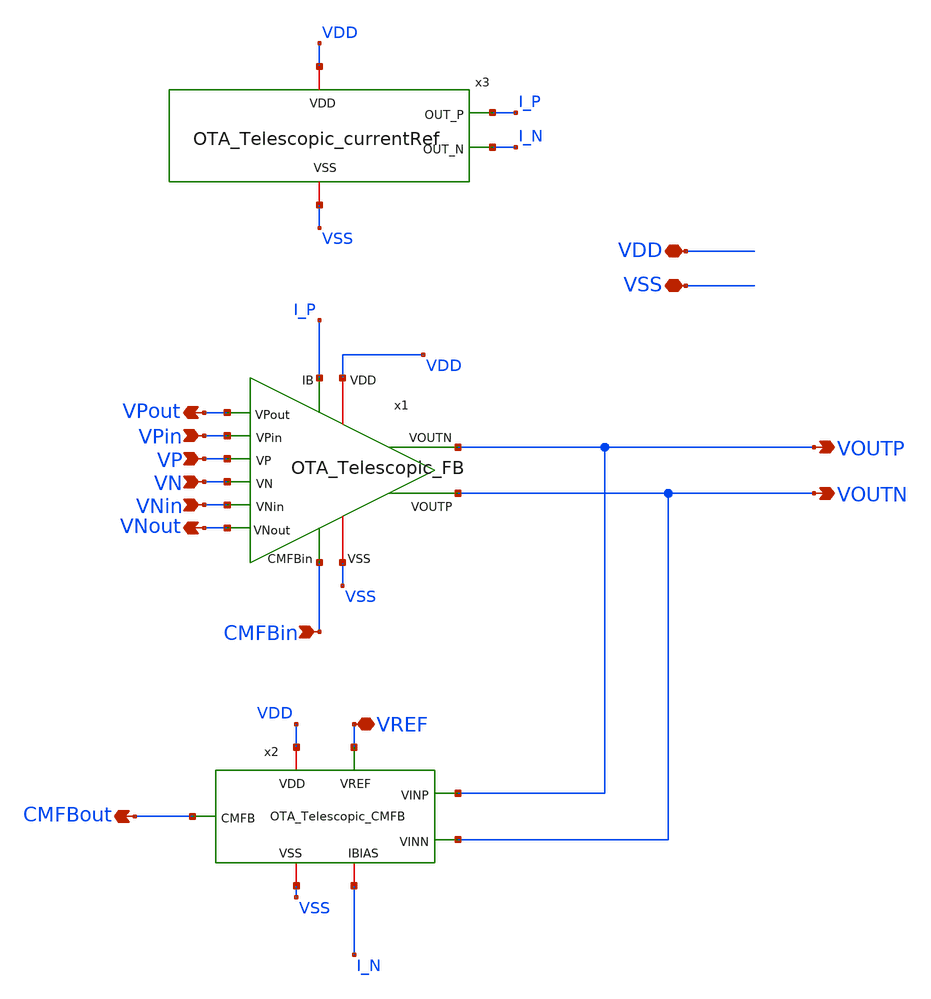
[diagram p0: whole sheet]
** sch_path: OTA_Telescopic_TEST/OTA_Telescopic_TOP_wp.sch
**.subckt OTA_Telescopic_TOP_wp VP VN VOUTP VOUTN VPin VNin VPout VNout VDD VSS VREF CMFBin CMFBout
*.ipin VP
*.ipin VN
*.opin VOUTP
*.opin VOUTN
*.ipin VPin
*.ipin VNin
*.opin VPout
*.opin VNout
*.iopin VDD
*.iopin VSS
*.iopin VREF
*.ipin CMFBin
*.opin CMFBout
x3 VDD I_P I_N VSS OTA_Telescopic_currentRef
x2 VDD VREF VOUTN VOUTP I_N CMFBout VSS OTA_Telescopic_CMFB
x1 I_P VPout VP VPin VOUTN VDD VOUTP VSS VNin VNout VN CMFBin OTA_Telescopic_FB
**.ends

* expanding   symbol:  OTA_Telescopic_currentRef.sym # of pins=4
** sym_path: OTA_Telescopic/OTA_Telescopic_currentRef.sym
** sch_path: OTA_Telescopic/OTA_Telescopic_currentRef.sch
.subckt OTA_Telescopic_currentRef VDD OUT_P OUT_N VSS
*.iopin VDD
*.iopin VSS
*.opin OUT_P
*.opin OUT_N
XM3 OUT_P OUT_P VDD VDD sg13_lv_pmos w=12u l=2.5u ng=2 m=1 mm_ok=1
XM2 OUT_P OUT_N net1 VSS sg13_lv_nmos w=12u l=6.4u ng=2 m=8 mm_ok=1
XM4 OUT_N OUT_P VDD VDD sg13_lv_pmos w=12u l=2.5u ng=2 m=1 mm_ok=1
XM1 OUT_N OUT_N VSS VSS sg13_lv_nmos w=12u l=6.4u ng=2 m=1 mm_ok=1
XM5 OUT_P OUT_P OUT_N VSS sg13_lv_nmos w=2u l=1u ng=1 m=1 mm_ok=1
XR2 net1 VSS VSS rppd w=1e-6 l=13.5e-6 m=1 b=0 mm_ok=1
.ends


* expanding   symbol:  OTA_Telescopic_CMFB.sym # of pins=7
** sym_path: OTA_Telescopic_CMFB.sym
** sch_path: OTA_Telescopic_CMFB.sch
.subckt OTA_Telescopic_CMFB VDD VREF VINN VINP IBIAS CMFB VSS
*.iopin VDD
*.iopin VSS
*.opin CMFB
*.ipin VREF
*.iopin IBIAS
*.ipin VINP
*.ipin VINN
XM0 IBIAS IBIAS VDD VDD sg13_lv_pmos w=6u l=0.7u ng=6 m=8 mm_ok=1
XM1 V1 IBIAS VDD VDD sg13_lv_pmos w=6u l=0.7u ng=6 m=24 mm_ok=1
XM2 V2 IBIAS VDD VDD sg13_lv_pmos w=6u l=0.7u ng=6 m=24 mm_ok=1
XM3 CMFB VINP V1 VDD sg13_lv_pmos w=8.995u l=0.35u ng=7 m=4 mm_ok=1
XM4 net1 VREF V1 VDD sg13_lv_pmos w=8.995u l=0.35u ng=7 m=4 mm_ok=1
XM5 net1 VREF V2 VDD sg13_lv_pmos w=8.995u l=0.35u ng=7 m=4 mm_ok=1
XM6 CMFB VINN V2 VDD sg13_lv_pmos w=8.995u l=0.35u ng=7 m=4 mm_ok=1
XM7 net1 net1 VSS VSS sg13_lv_nmos w=29.97u l=0.20u ng=9 m=1 mm_ok=1
XM8 CMFB CMFB VSS VSS sg13_lv_nmos w=29.97u l=0.20u ng=9 m=1 mm_ok=1
.ends


* expanding   symbol:  OTA_Telescopic_FB.sym # of pins=12
** sym_path: OTA_Telescopic_FB.sym
** sch_path: OTA_Telescopic_FB.sch
.subckt OTA_Telescopic_FB IB VPout VP VPin VOUTP VDD VOUTN VSS VNin VNout VN CMFBin
*.ipin VP
*.ipin VN
*.opin VOUTP
*.opin VOUTN
*.ipin VPin
*.ipin VNin
*.opin VPout
*.opin VNout
*.iopin VDD
*.iopin VSS
*.ipin CMFBin
*.ipin IB
x1 VDD CMFBin VOUTN VOUTP VPin VNin VSS IB OTA_Telescopic_core
XR3 VNout VN VSS rppd w=0.6e-6 l=6.73e-6 m=1 b=0 mm_ok=1
XR4 VP VPout VSS rppd w=0.6e-6 l=6.73e-6 m=1 b=0 mm_ok=1
XR5 VPout VOUTP VSS rppd w=0.6e-6 l=19e-6 m=1 b=0 mm_ok=1
XR2 VNout VOUTN VSS rppd w=0.6e-6 l=19e-6 m=1 b=0 mm_ok=1
.ends


* expanding   symbol:  OTA_Telescopic_core.sym # of pins=8
** sym_path: OTA_Telescopic_core.sym
** sch_path: OTA_Telescopic_core.sch
.subckt OTA_Telescopic_core VDD CMFB VOUTP VOUTN VINP VINN VSS IB
*.iopin VDD
*.iopin VSS
*.ipin VINP
*.ipin VINN
*.opin VOUTN
*.opin VOUTP
*.ipin CMFB
*.iopin IB
V2 VB2 VSS 1.5
V3 VB3 VSS 0.7
V4 VB4 VSS 0.49409
V1 VB5 VSS 1.15
* noconn VB2
* noconn VB3
* noconn VB4
* noconn VB5
V5 VB VSS 0.90204
* noconn VB
XM15 VB55 VB55 VDD VDD sg13_lv_pmos w=1.4u l=0.35u ng=1 m=8 mm_ok=1
XM17 VB33 VB33 VDD VDD sg13_lv_pmos w=2.05u l=0.35u ng=1 m=1 mm_ok=1
XM18 VB22 VB33 VDD VDD sg13_lv_pmos w=2.05u l=0.35u ng=1 m=1 mm_ok=1
XM9 VOUTP Vo1 VDD VDD sg13_lv_pmos w=1.37u l=0.35u ng=1 m=250 mm_ok=1
XM7 Vx1 VB55 VDD VDD sg13_lv_pmos w=7u l=0.7u ng=1 m=30 mm_ok=1
XM5 Vo1 VB33 Vx1 VDD sg13_lv_pmos w=4.05u l=0.5u ng=1 m=30 mm_ok=1
XM8 Vx2 VB55 VDD VDD sg13_lv_pmos w=7u l=0.7u ng=1 m=30 mm_ok=1
XM6 Vo2 VB33 Vx2 VDD sg13_lv_pmos w=4.05u l=0.5u ng=1 m=30 mm_ok=1
XM10 VOUTN Vo2 VDD VDD sg13_lv_pmos w=1.37u l=0.35u ng=1 m=250 mm_ok=1
XM13 IB IB VSS VSS sg13_lv_nmos w=4.8u l=1.06u ng=1 m=1 mm_ok=1
XM14 VB55 IB VSS VSS sg13_lv_nmos w=4.8u l=1.06u ng=1 m=1 mm_ok=1
XM16 VB33 IB VSS VSS sg13_lv_nmos w=4.8u l=1.06u ng=1 m=1 mm_ok=1
XM19 VB22 VB22 VSS VSS sg13_lv_nmos w=0.5u l=0.8u ng=1 m=1 mm_ok=1
XM11 VOUTP IB VSS VSS sg13_lv_nmos w=4.8u l=1.06u ng=1 m=55 mm_ok=1
XM0 P CMFB VSS VSS sg13_lv_nmos w=30u l=0.20u ng=9 m=6 mm_ok=1
XM3 Vo1 VB22 Vy1 VSS sg13_lv_nmos w=1.9u l=0.16u ng=1 m=30 mm_ok=1
XM1 Vy1 VINP P VSS sg13_lv_nmos w=1.1u l=0.15u ng=1 m=30 mm_ok=1
XM4 Vo2 VB22 Vy2 VSS sg13_lv_nmos w=1.9u l=0.16u ng=1 m=30 mm_ok=1
XM2 Vy2 VINN P VSS sg13_lv_nmos w=1.1u l=0.15u ng=1 m=30 mm_ok=1
XM12 VOUTN IB VSS VSS sg13_lv_nmos w=4.8u l=1.06u ng=1 m=55 mm_ok=1
XR3 net1 VOUTP VSS rppd w=1.5e-6 l=0.55e-6 m=1 b=0 mm_ok=1
XR1 VOUTN net2 VSS rppd w=1.5e-6 l=0.55e-6 m=1 b=0 mm_ok=1
XC3 Vo2 net2 cap_cmim w=21.4e-6 l=21.4e-6 m=1 mm_ok=1
XC1 Vo1 net1 cap_cmim w=21.4e-6 l=21.4e-6 m=1 mm_ok=1
.ends

.end
